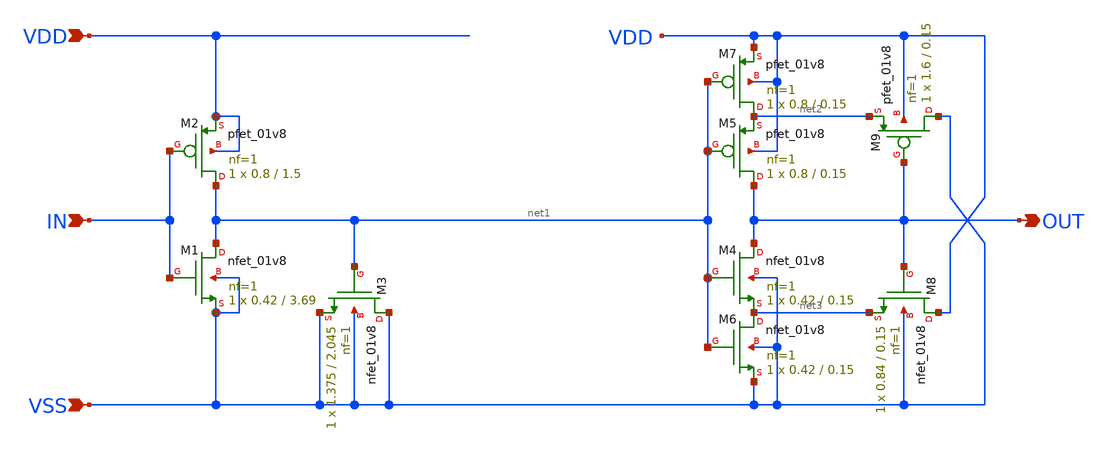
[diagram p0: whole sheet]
** sch_path: hgu/xschem/hgu_delay_no_code.sch
**.subckt hgu_delay_no_code IN VDD VSS OUT
*.ipin IN
*.ipin VDD
*.ipin VSS
*.opin OUT
XM1 net1 IN VSS VSS sky130_fd_pr__nfet_01v8 L=3.69 W=0.42 nf=1 ad='int((nf+1)/2) * W/nf * 0.29' as='int((nf+2)/2) * W/nf * 0.29'
+ pd='2*int((nf+1)/2) * (W/nf + 0.29)' ps='2*int((nf+2)/2) * (W/nf + 0.29)' nrd='0.29 / W' nrs='0.29 / W'
+ sa=0 sb=0 sd=0 mult=1 m=1
XM2 net1 IN VDD VDD sky130_fd_pr__pfet_01v8 L=1.5 W=0.8 nf=1 ad='int((nf+1)/2) * W/nf * 0.29' as='int((nf+2)/2) * W/nf * 0.29'
+ pd='2*int((nf+1)/2) * (W/nf + 0.29)' ps='2*int((nf+2)/2) * (W/nf + 0.29)' nrd='0.29 / W' nrs='0.29 / W'
+ sa=0 sb=0 sd=0 mult=1 m=1
XM3 VSS net1 VSS VSS sky130_fd_pr__nfet_01v8 L=2.045 W=1.375 nf=1 ad='int((nf+1)/2) * W/nf * 0.29' as='int((nf+2)/2) * W/nf * 0.29'
+ pd='2*int((nf+1)/2) * (W/nf + 0.29)' ps='2*int((nf+2)/2) * (W/nf + 0.29)' nrd='0.29 / W' nrs='0.29 / W'
+ sa=0 sb=0 sd=0 mult=1 m=1
XM4 OUT net1 net3 VSS sky130_fd_pr__nfet_01v8 L=0.15 W=0.42 nf=1 ad='int((nf+1)/2) * W/nf * 0.29' as='int((nf+2)/2) * W/nf * 0.29'
+ pd='2*int((nf+1)/2) * (W/nf + 0.29)' ps='2*int((nf+2)/2) * (W/nf + 0.29)' nrd='0.29 / W' nrs='0.29 / W'
+ sa=0 sb=0 sd=0 mult=1 m=1
XM5 OUT net1 net2 VDD sky130_fd_pr__pfet_01v8 L=0.15 W=0.8 nf=1 ad='int((nf+1)/2) * W/nf * 0.29' as='int((nf+2)/2) * W/nf * 0.29'
+ pd='2*int((nf+1)/2) * (W/nf + 0.29)' ps='2*int((nf+2)/2) * (W/nf + 0.29)' nrd='0.29 / W' nrs='0.29 / W'
+ sa=0 sb=0 sd=0 mult=1 m=1
XM6 net3 net1 VSS VSS sky130_fd_pr__nfet_01v8 L=0.15 W=0.42 nf=1 ad='int((nf+1)/2) * W/nf * 0.29' as='int((nf+2)/2) * W/nf * 0.29'
+ pd='2*int((nf+1)/2) * (W/nf + 0.29)' ps='2*int((nf+2)/2) * (W/nf + 0.29)' nrd='0.29 / W' nrs='0.29 / W'
+ sa=0 sb=0 sd=0 mult=1 m=1
XM7 net2 net1 VDD VDD sky130_fd_pr__pfet_01v8 L=0.15 W=0.8 nf=1 ad='int((nf+1)/2) * W/nf * 0.29' as='int((nf+2)/2) * W/nf * 0.29'
+ pd='2*int((nf+1)/2) * (W/nf + 0.29)' ps='2*int((nf+2)/2) * (W/nf + 0.29)' nrd='0.29 / W' nrs='0.29 / W'
+ sa=0 sb=0 sd=0 mult=1 m=1
XM8 VDD OUT net3 VSS sky130_fd_pr__nfet_01v8 L=0.15 W=0.84 nf=1 ad='int((nf+1)/2) * W/nf * 0.29' as='int((nf+2)/2) * W/nf * 0.29'
+ pd='2*int((nf+1)/2) * (W/nf + 0.29)' ps='2*int((nf+2)/2) * (W/nf + 0.29)' nrd='0.29 / W' nrs='0.29 / W'
+ sa=0 sb=0 sd=0 mult=1 m=1
XM9 VSS OUT net2 VDD sky130_fd_pr__pfet_01v8 L=0.15 W=1.6 nf=1 ad='int((nf+1)/2) * W/nf * 0.29' as='int((nf+2)/2) * W/nf * 0.29'
+ pd='2*int((nf+1)/2) * (W/nf + 0.29)' ps='2*int((nf+2)/2) * (W/nf + 0.29)' nrd='0.29 / W' nrs='0.29 / W'
+ sa=0 sb=0 sd=0 mult=1 m=1
**.ends
.end
